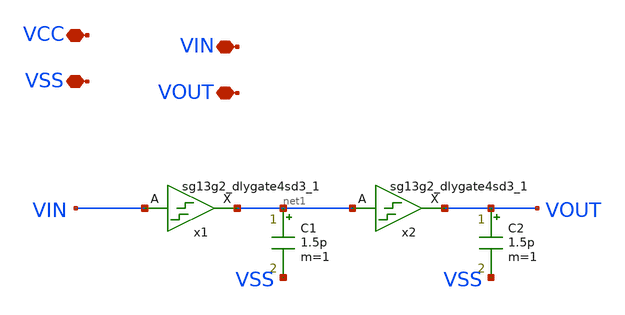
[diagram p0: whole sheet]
** sch_path: ChipUSM_AnalogTrack24/large_delay/large_delayRC_v1p1.sch
**.subckt large_delayRC_v1p1 VIN VOUT VCC VSS
*.iopin VIN
*.iopin VOUT
*.iopin VCC
*.iopin VSS
x1 net1 VIN VCC VSS sg13g2_dlygate4sd3_1
x2 VOUT net1 VCC VSS sg13g2_dlygate4sd3_1
C1 net1 VSS 1.5p m=1
C2 VOUT VSS 1.5p m=1
**.ends

* expanding   symbol:  sg13g2_stdcells/sg13g2_dlygate4sd3_1.sym # of pins=2
** sym_path: sg13g2_stdcells/sg13g2_dlygate4sd3_1.sym
** sch_path: sg13g2_stdcells/sg13g2_dlygate4sd3_1.sch
.subckt sg13g2_dlygate4sd3_1 X A VDD VSS
*.ipin A
*.opin X
*.iopin VDD
*.iopin VSS
XM1 net3 A VSS VSS sg13_lv_nmos w=420.00n l=130.00n ng=1 m=1 mm_ok=1
XM2 net1 net3 VSS VSS sg13_lv_nmos w=420.00n l=500.0n ng=1 m=1 mm_ok=1
XM3 net2 net1 VSS VSS sg13_lv_nmos w=420.00n l=500.0n ng=1 m=1 mm_ok=1
XM4 X net2 VSS VSS sg13_lv_nmos w=740.00n l=130.00n ng=1 m=1 mm_ok=1
XM5 net3 A VDD VDD sg13_lv_pmos w=420.00n l=130.00n ng=1 m=1 mm_ok=1
XM6 net1 net3 VDD VDD sg13_lv_pmos w=1.000u l=500.0n ng=1 m=1 mm_ok=1
XM7 net2 net1 VDD VDD sg13_lv_pmos w=1.000u l=500.0n ng=1 m=1 mm_ok=1
XM8 X net2 VDD VDD sg13_lv_pmos w=1.12u l=130.00n ng=1 m=1 mm_ok=1
.ends

.end
